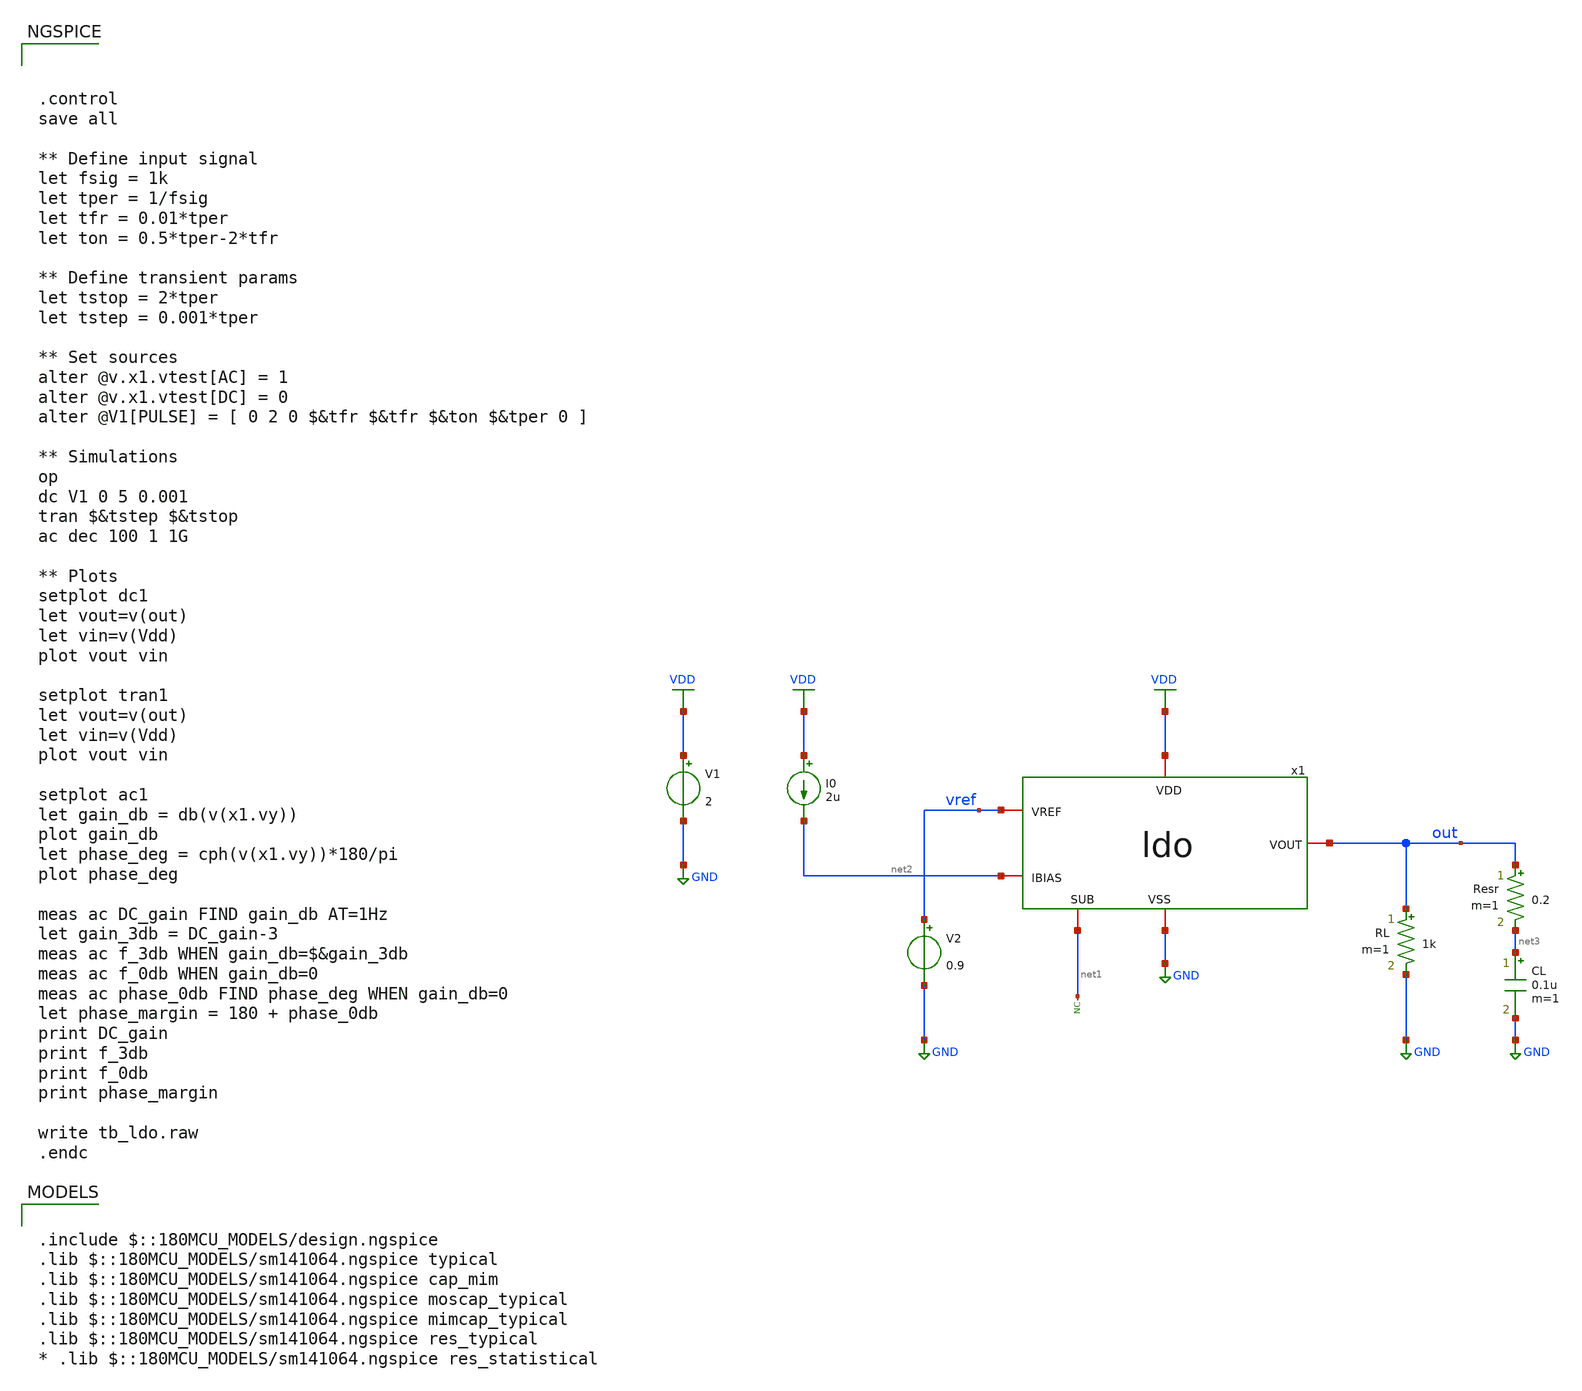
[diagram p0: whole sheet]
** sch_path: designs/libs/tb_ldo/tb_ldo/tb_ldo/tb_ldo.sch
**.subckt tb_ldo
* noconn #net1
RL out GND 1k m=1
V1 VDD GND 2
V2 vref GND 0.9
I0 VDD net2 2u
CL net3 GND 0.1u m=1
Resr out net3 0.2 m=1
x1 VDD vref out net2 net1 GND ldo
**** begin user architecture code

.include $::180MCU_MODELS/design.ngspice
.lib $::180MCU_MODELS/sm141064.ngspice typical
.lib $::180MCU_MODELS/sm141064.ngspice cap_mim
.lib $::180MCU_MODELS/sm141064.ngspice moscap_typical
.lib $::180MCU_MODELS/sm141064.ngspice mimcap_typical
.lib $::180MCU_MODELS/sm141064.ngspice res_typical
* .lib $::180MCU_MODELS/sm141064.ngspice res_statistical




.control
save all

** Define input signal
let fsig = 1k
let tper = 1/fsig
let tfr = 0.01*tper
let ton = 0.5*tper-2*tfr

** Define transient params
let tstop = 2*tper
let tstep = 0.001*tper

** Set sources
alter @v.x1.vtest[AC] = 1
alter @v.x1.vtest[DC] = 0
alter @V1[PULSE] = [ 0 2 0 $&tfr $&tfr $&ton $&tper 0 ]

** Simulations
op
dc V1 0 5 0.001
tran $&tstep $&tstop
ac dec 100 1 1G

** Plots
setplot dc1
let vout=v(out)
let vin=v(Vdd)
plot vout vin

setplot tran1
let vout=v(out)
let vin=v(Vdd)
plot vout vin

setplot ac1
let gain_db = db(v(x1.vy))
plot gain_db
let phase_deg = cph(v(x1.vy))*180/pi
plot phase_deg

meas ac DC_gain FIND gain_db AT=1Hz
let gain_3db = DC_gain-3
meas ac f_3db WHEN gain_db=$&gain_3db
meas ac f_0db WHEN gain_db=0
meas ac phase_0db FIND phase_deg WHEN gain_db=0
let phase_margin = 180 + phase_0db
print DC_gain
print f_3db
print f_0db
print phase_margin

write tb_ldo.raw
.endc


**** end user architecture code
**.ends
.GLOBAL GND
.GLOBAL VDD
.end
